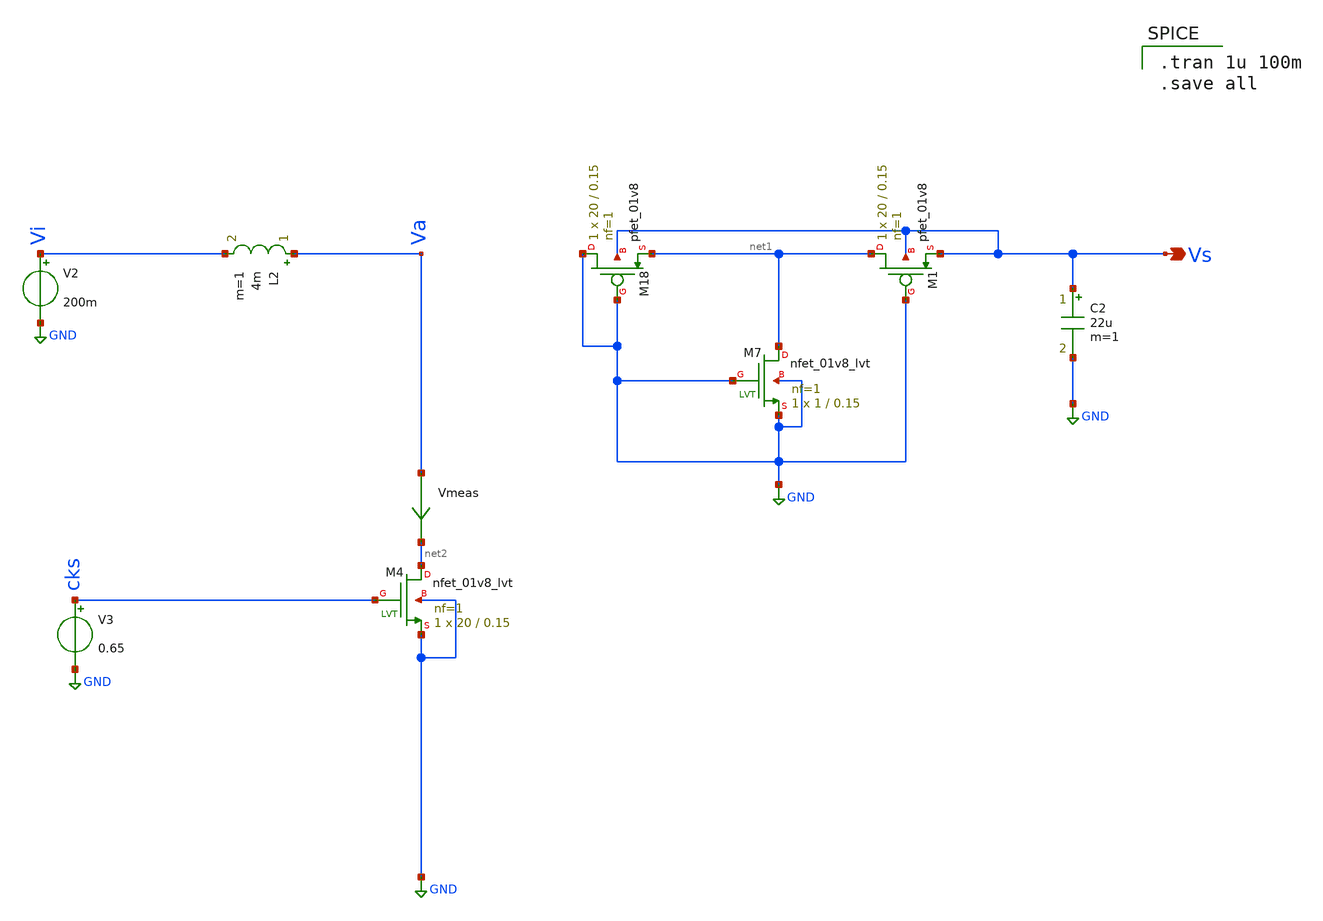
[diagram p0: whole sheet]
** sch_path: Blocks/Startup Converter/Boost_Conv1.sch
**.subckt Boost_Conv1 Vs
*.opin Vs
L2 Va Vi 4m m=1
C2 Vs GND 22u m=1
XM4 net2 cks GND GND sky130_fd_pr__nfet_01v8_lvt L=0.15 W=20 nf=1 ad='int((nf+1)/2) * W/nf * 0.29' as='int((nf+2)/2) * W/nf * 0.29'
+ pd='2*int((nf+1)/2) * (W/nf + 0.29)' ps='2*int((nf+2)/2) * (W/nf + 0.29)' nrd='0.29 / W' nrs='0.29 / W'
+ sa=0 sb=0 sd=0 mult=1 m=1
XM7 net1 GND GND GND sky130_fd_pr__nfet_01v8_lvt L=0.15 W=1 nf=1 ad='int((nf+1)/2) * W/nf * 0.29' as='int((nf+2)/2) * W/nf * 0.29'
+ pd='2*int((nf+1)/2) * (W/nf + 0.29)' ps='2*int((nf+2)/2) * (W/nf + 0.29)' nrd='0.29 / W' nrs='0.29 / W'
+ sa=0 sb=0 sd=0 mult=1 m=1
V2 Vi GND 200m
XM18 GND GND net1 Vs sky130_fd_pr__pfet_01v8 L=0.15 W=20 nf=1 ad='int((nf+1)/2) * W/nf * 0.29' as='int((nf+2)/2) * W/nf * 0.29'
+ pd='2*int((nf+1)/2) * (W/nf + 0.29)' ps='2*int((nf+2)/2) * (W/nf + 0.29)' nrd='0.29 / W' nrs='0.29 / W'
+ sa=0 sb=0 sd=0 mult=1 m=1
XM1 net1 GND Vs Vs sky130_fd_pr__pfet_01v8 L=0.15 W=20 nf=1 ad='int((nf+1)/2) * W/nf * 0.29' as='int((nf+2)/2) * W/nf * 0.29'
+ pd='2*int((nf+1)/2) * (W/nf + 0.29)' ps='2*int((nf+2)/2) * (W/nf + 0.29)' nrd='0.29 / W' nrs='0.29 / W'
+ sa=0 sb=0 sd=0 mult=1 m=1
V3 cks GND 0.65
Vmeas Va net2 0
.save i(vmeas)
**** begin user architecture code

** opencircuitdesign pdks install
.lib $::SKYWATER_MODELS/sky130.lib.spice tt



.tran 1u 100m
.save all

**** end user architecture code
**.ends
.GLOBAL GND
.end
